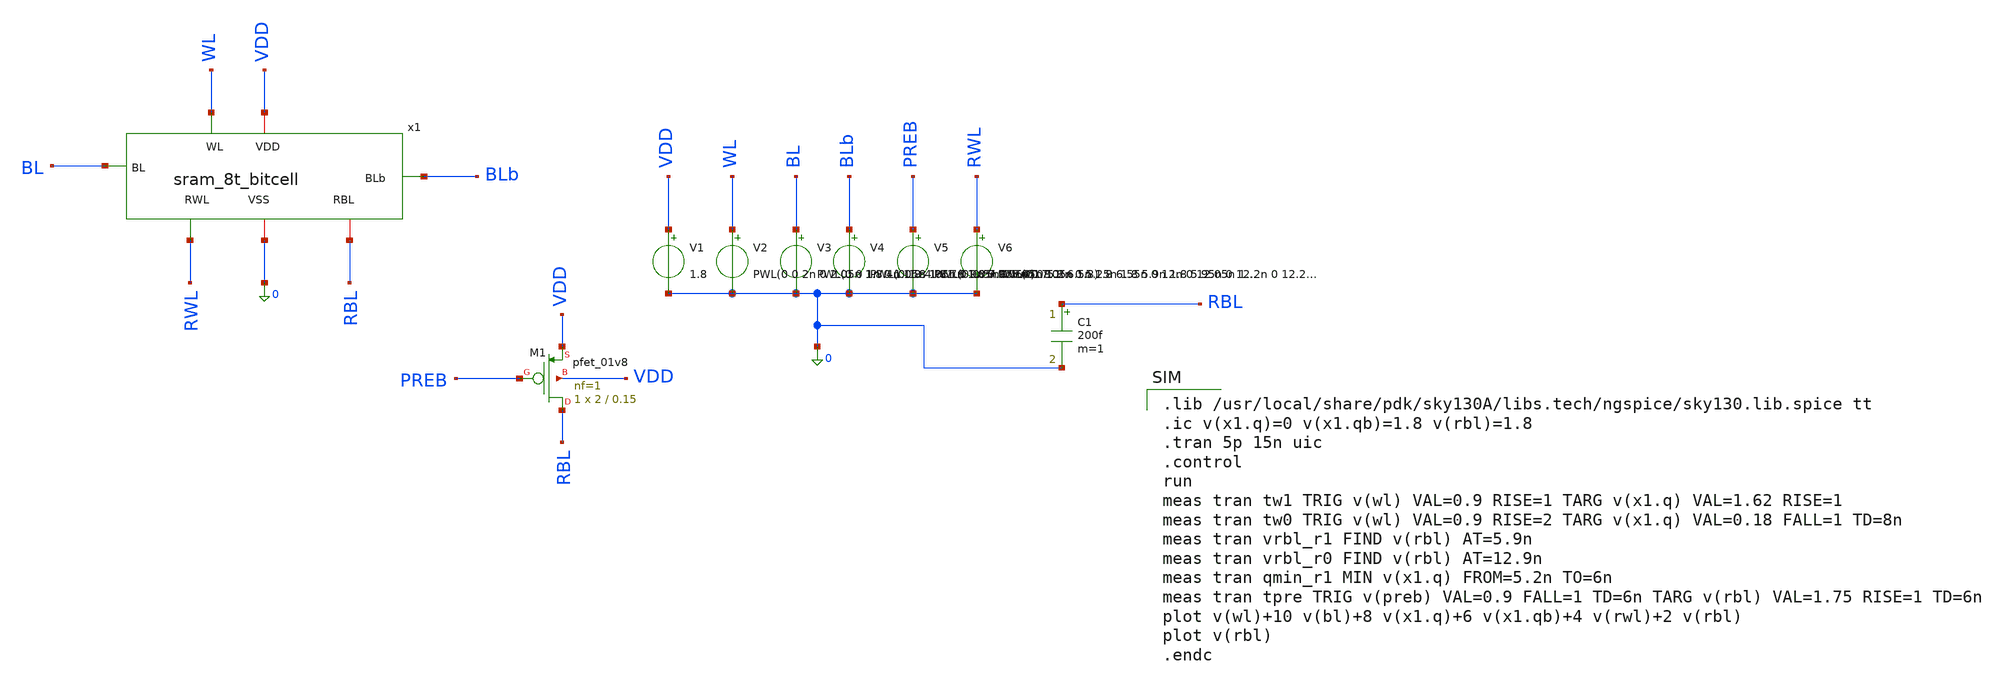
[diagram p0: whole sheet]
** sch_path: schematics/sram_8t_bitcell_tb.sch
**.subckt sram_8t_bitcell_tb
x1 VDD WL BL BLb RWL 0 RBL sram_8t_bitcell
V1 VDD 0 1.8
V2 WL 0 PWL(0 0 2n 0 2.05n 1.8 4n 1.8 4.05n 0 9n 0 9.05n 1.8 11n 1.8 11.05n 0)
V3 BL 0 PWL(0 0 1n 0 1.05n 1.8 7n 1.8 7.05n 0)
V4 BLb 0 PWL(0 1.8 1n 1.8 1.05n 0 7n 0 7.05n 1.8)
V5 PREB 0 PWL(0 0 5n 0 5.05n 1.8 6.5n 1.8 6.55n 0 12n 0 12.05n 1.8 13.5n 1.8 13.55n 0)
V6 RWL 0 PWL(0 0 5.2n 0 5.25n 1.8 5.9n 1.8 5.95n 0 12.2n 0 12.25n 1.8 12.9n 1.8 12.95n 0)
XM1 RBL PREB VDD VDD sky130_fd_pr__pfet_01v8 L=0.15 W=2 nf=1 ad='int((1 + 1)/2) * 2 / 1 * 0.29' as='int((1 + 2)/2) * 2 / 1 * 0.29'
+ pd='2*int((1 + 1)/2) * (2 / 1 + 0.29)' ps='2*int((1 + 2)/2) * (2 / 1 + 0.29)' nrd='0.29 / 2 ' nrs='0.29 / 2 '
+ sa=0 sb=0 sd=0 mult=1 m=1
C1 RBL 0 200f m=1
**** begin user architecture code

.lib /usr/local/share/pdk/sky130A/libs.tech/ngspice/sky130.lib.spice tt
.ic v(x1.q)=0 v(x1.qb)=1.8 v(rbl)=1.8
.tran 5p 15n uic
.control
run
meas tran tw1 TRIG v(wl) VAL=0.9 RISE=1 TARG v(x1.q) VAL=1.62 RISE=1
meas tran tw0 TRIG v(wl) VAL=0.9 RISE=2 TARG v(x1.q) VAL=0.18 FALL=1 TD=8n
meas tran vrbl_r1 FIND v(rbl) AT=5.9n
meas tran vrbl_r0 FIND v(rbl) AT=12.9n
meas tran qmin_r1 MIN v(x1.q) FROM=5.2n TO=6n
meas tran tpre TRIG v(preb) VAL=0.9 FALL=1 TD=6n TARG v(rbl) VAL=1.75 RISE=1 TD=6n
plot v(wl)+10 v(bl)+8 v(x1.q)+6 v(x1.qb)+4 v(rwl)+2 v(rbl)
plot v(rbl)
.endc


**** end user architecture code
**.ends
.end
